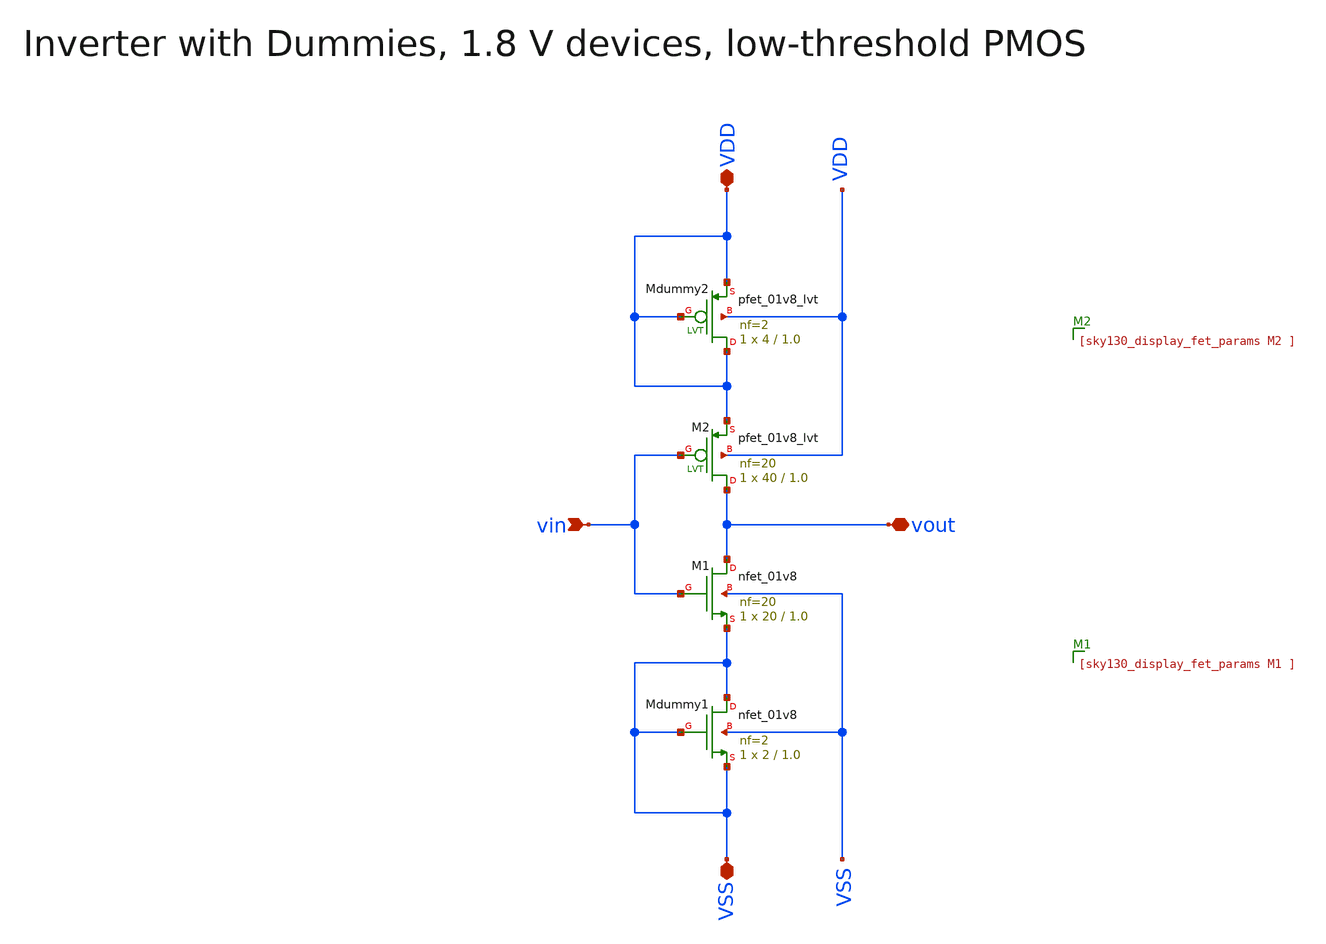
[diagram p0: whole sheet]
** sch_path: macros/inverter/schematic/xschem/inverter.sch
**.subckt inverter vin VDD VSS vout
*.ipin vin
*.iopin VDD
*.iopin VSS
*.iopin vout
XMdummy1 VSS VSS VSS VSS sky130_fd_pr__nfet_01v8 L=1.0 W=2 nf=2 ad='int((2 + 1)/2) * 2 / 2 * 0.29' as='int((2 + 2)/2) * 2 / 2 * 0.29'
+ pd='2*int((2 + 1)/2) * (2 / 2 + 0.29)' ps='2*int((2 + 2)/2) * (2 / 2 + 0.29)' nrd='0.29 / 2 ' nrs='0.29 / 2 '
+ sa=0 sb=0 sd=0 mult=1 m=1
XMdummy2 VDD VDD VDD VDD sky130_fd_pr__pfet_01v8_lvt L=1.0 W=4 nf=2 ad='int((2 + 1)/2) * 4 / 2 * 0.29'
+ as='int((2 + 2)/2) * 4 / 2 * 0.29' pd='2*int((2 + 1)/2) * (4 / 2 + 0.29)' ps='2*int((2 + 2)/2) * (4 / 2 + 0.29)'
+ nrd='0.29 / 4 ' nrs='0.29 / 4 ' sa=0 sb=0 sd=0 mult=1 m=1
XM1 vout vin VSS VSS sky130_fd_pr__nfet_01v8 L=1.0 W=20 nf=20 ad='int((20 + 1)/2) * 20 / 20 * 0.29' as='int((20 + 2)/2) * 20 / 20 * 0.29'
+ pd='2*int((20 + 1)/2) * (20 / 20 + 0.29)' ps='2*int((20 + 2)/2) * (20 / 20 + 0.29)' nrd='0.29 / 20 '
+ nrs='0.29 / 20 ' sa=0 sb=0 sd=0 mult=1 m=1
XM2 vout vin VDD VDD sky130_fd_pr__pfet_01v8_lvt L=1.0 W=40 nf=20 ad='int((20 + 1)/2) * 40 / 20 * 0.29'
+ as='int((20 + 2)/2) * 40 / 20 * 0.29' pd='2*int((20 + 1)/2) * (40 / 20 + 0.29)' ps='2*int((20 + 2)/2) * (40 / 20 + 0.29)'
+ nrd='0.29 / 40 ' nrs='0.29 / 40 ' sa=0 sb=0 sd=0 mult=1 m=1
**.ends
.end
